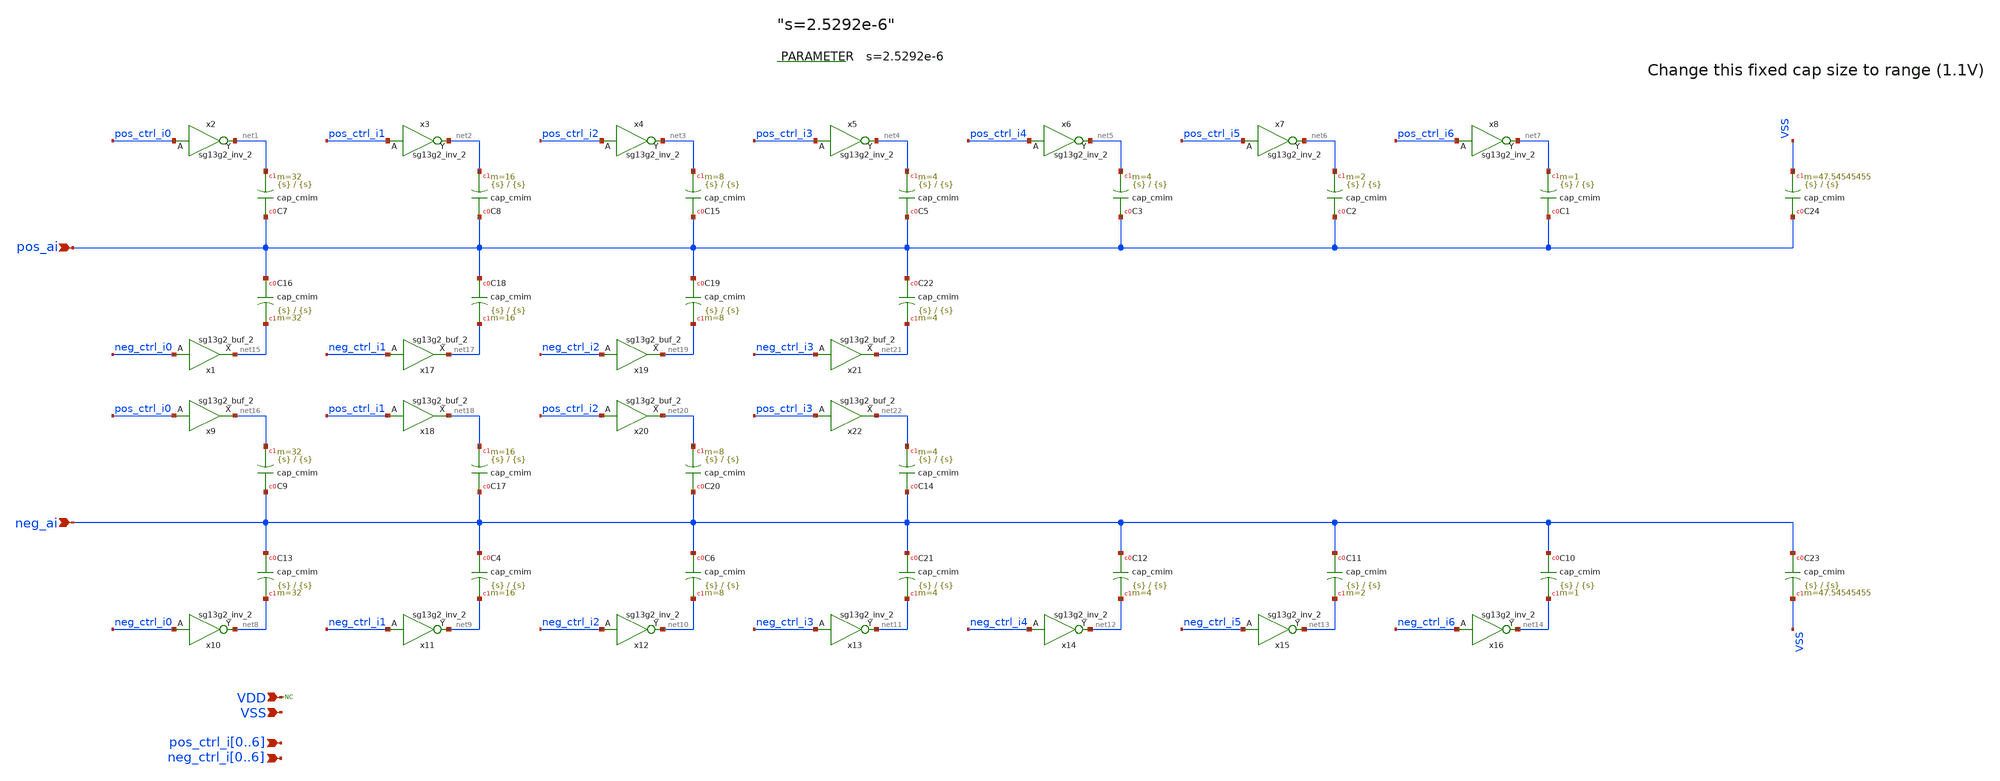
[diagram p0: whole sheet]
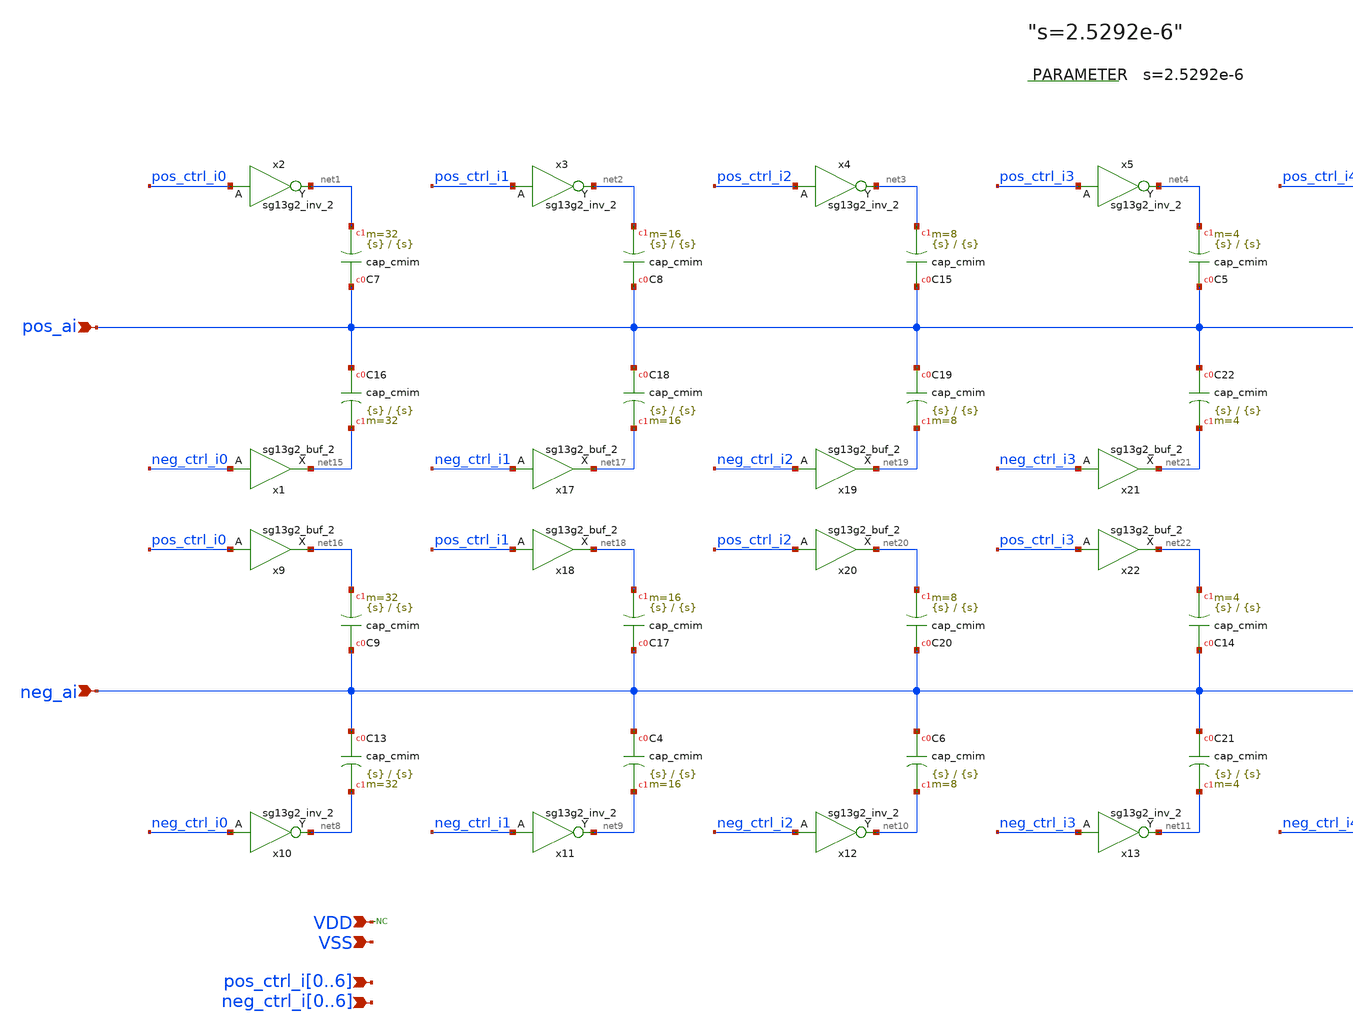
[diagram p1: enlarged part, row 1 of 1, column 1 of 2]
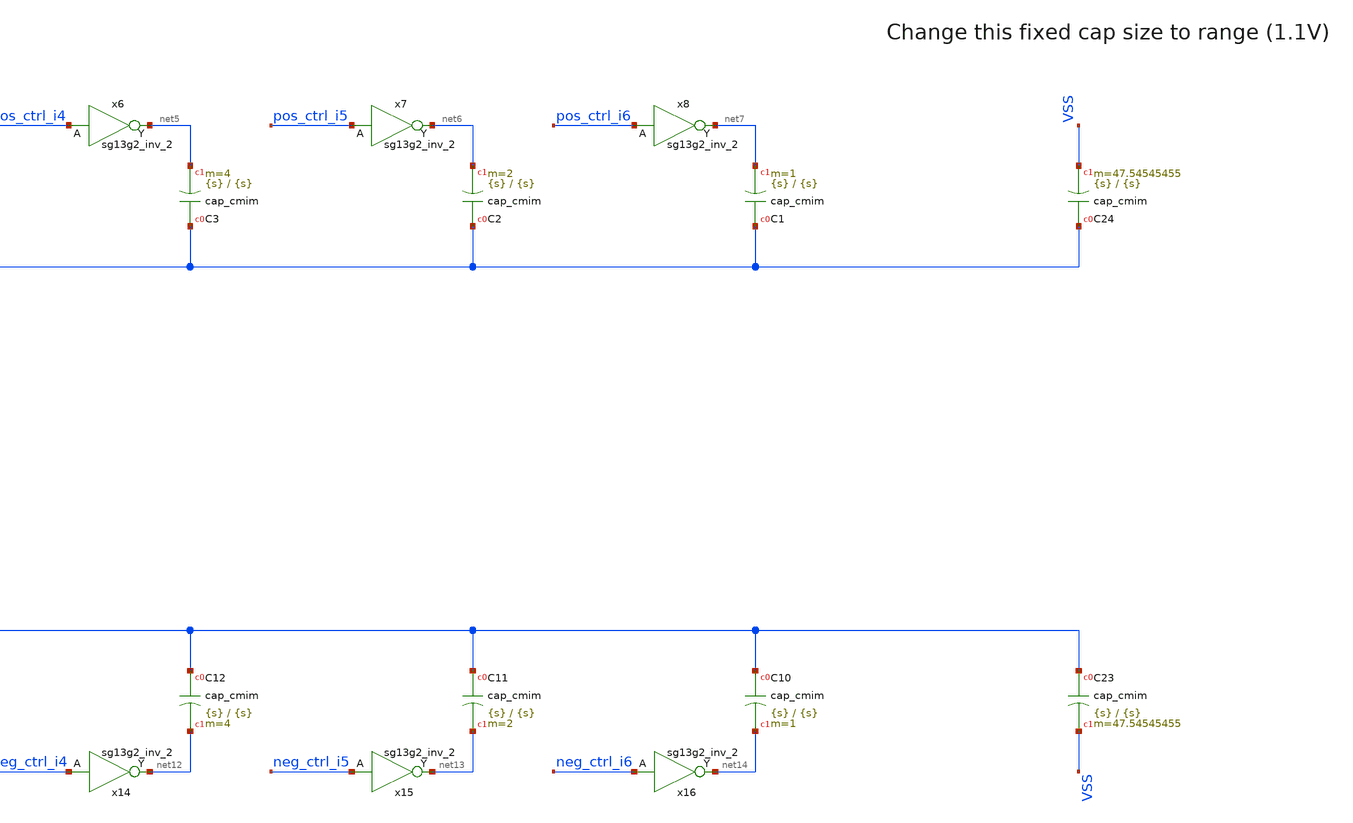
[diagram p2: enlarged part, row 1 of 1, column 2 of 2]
** sch_path: xschem/cdac.sch
* IHP-GmbH/IHP-Open-PDK/ihp-sg13g2/libs.tech/xschem/sg13g2_stdcells/sg13g2_inv_2.sch:
* Copyright 2023 IHP PDK Authors
* Licensed under the Apache License, Version 2.0 (the "License");
**.subckt cdac pos_ai VSS VDD neg_ai
*+ pos_ctrl_i0,pos_ctrl_i1,pos_ctrl_i2,pos_ctrl_i3,pos_ctrl_i4,pos_ctrl_i5,pos_ctrl_i6 neg_ctrl_i0,neg_ctrl_i1,neg_ctrl_i2,neg_ctrl_i3,neg_ctrl_i4,neg_ctrl_i5,neg_ctrl_i6
*.ipin pos_ai
*.ipin VSS
*.ipin VDD
*.ipin neg_ai
*.ipin pos_ctrl_i0,pos_ctrl_i1,pos_ctrl_i2,pos_ctrl_i3,pos_ctrl_i4,pos_ctrl_i5,pos_ctrl_i6
*.ipin neg_ctrl_i0,neg_ctrl_i1,neg_ctrl_i2,neg_ctrl_i3,neg_ctrl_i4,neg_ctrl_i5,neg_ctrl_i6
x2 net1 pos_ctrl_i0 VDD VSS sg13g2_inv_2
x3 net2 pos_ctrl_i1 VDD VSS sg13g2_inv_2
x4 net3 pos_ctrl_i2 VDD VSS sg13g2_inv_2
x5 net4 pos_ctrl_i3 VDD VSS sg13g2_inv_2
x6 net5 pos_ctrl_i4 VDD VSS sg13g2_inv_2
x7 net6 pos_ctrl_i5 VDD VSS sg13g2_inv_2
x8 net7 pos_ctrl_i6 VDD VSS sg13g2_inv_2
XC1 pos_ai net7 cap_cmim w={s} l={s} m=1 mm_ok=1
XC2 pos_ai net6 cap_cmim w={s} l={s} m=2 mm_ok=1
XC3 pos_ai net5 cap_cmim w={s} l={s} m=4 mm_ok=1
x10 net8 neg_ctrl_i0 VDD VSS sg13g2_inv_2
x11 net9 neg_ctrl_i1 VDD VSS sg13g2_inv_2
x12 net10 neg_ctrl_i2 VDD VSS sg13g2_inv_2
x13 net11 neg_ctrl_i3 VDD VSS sg13g2_inv_2
x14 net12 neg_ctrl_i4 VDD VSS sg13g2_inv_2
x15 net13 neg_ctrl_i5 VDD VSS sg13g2_inv_2
x16 net14 neg_ctrl_i6 VDD VSS sg13g2_inv_2
XC10 neg_ai net14 cap_cmim w={s} l={s} m=1 mm_ok=1
XC11 neg_ai net13 cap_cmim w={s} l={s} m=2 mm_ok=1
XC12 neg_ai net12 cap_cmim w={s} l={s} m=4 mm_ok=1
* noconn VDD
.param s=2.5292e-6
x1 net15 neg_ctrl_i0 VDD VSS sg13g2_buf_2
x9 net16 pos_ctrl_i0 VDD VSS sg13g2_buf_2
XC7 pos_ai net1 cap_cmim w={s} l={s} m=32 mm_ok=1
XC9 neg_ai net16 cap_cmim w={s} l={s} m=32 mm_ok=1
XC13 neg_ai net8 cap_cmim w={s} l={s} m=32 mm_ok=1
XC16 pos_ai net15 cap_cmim w={s} l={s} m=32 mm_ok=1
x17 net17 neg_ctrl_i1 VDD VSS sg13g2_buf_2
x18 net18 pos_ctrl_i1 VDD VSS sg13g2_buf_2
XC17 neg_ai net18 cap_cmim w={s} l={s} m=16 mm_ok=1
XC18 pos_ai net17 cap_cmim w={s} l={s} m=16 mm_ok=1
XC4 neg_ai net9 cap_cmim w={s} l={s} m=16 mm_ok=1
XC8 pos_ai net2 cap_cmim w={s} l={s} m=16 mm_ok=1
x19 net19 neg_ctrl_i2 VDD VSS sg13g2_buf_2
x20 net20 pos_ctrl_i2 VDD VSS sg13g2_buf_2
XC19 pos_ai net19 cap_cmim w={s} l={s} m=8 mm_ok=1
XC6 neg_ai net10 cap_cmim w={s} l={s} m=8 mm_ok=1
XC15 pos_ai net3 cap_cmim w={s} l={s} m=8 mm_ok=1
XC20 neg_ai net20 cap_cmim w={s} l={s} m=8 mm_ok=1
x21 net21 neg_ctrl_i3 VDD VSS sg13g2_buf_2
x22 net22 pos_ctrl_i3 VDD VSS sg13g2_buf_2
XC5 pos_ai net4 cap_cmim w={s} l={s} m=4 mm_ok=1
XC14 neg_ai net22 cap_cmim w={s} l={s} m=4 mm_ok=1
XC21 neg_ai net11 cap_cmim w={s} l={s} m=4 mm_ok=1
XC22 pos_ai net21 cap_cmim w={s} l={s} m=4 mm_ok=1
XC23 neg_ai VSS cap_cmim w={s} l={s} m=47.54545455 mm_ok=1
XC24 pos_ai VSS cap_cmim w={s} l={s} m=47.54545455 mm_ok=1
**.ends

* expanding   symbol:  sg13g2_stdcells/sg13g2_inv_2.sym # of pins=2
** sym_path: sg13g2_stdcells/sg13g2_inv_2.sym
** sch_path: sg13g2_stdcells/sg13g2_inv_2.sch
.subckt sg13g2_inv_2 Y A VDD VSS
*.opin Y
*.ipin A
*.iopin VDD
*.iopin VSS
XM1 Y A VSS VSS sg13_lv_nmos w=1.48u l=130.00n ng=2 m=1 mm_ok=1
XM2 Y A VDD VDD sg13_lv_pmos w=2.24u l=130.00n ng=2 m=1 mm_ok=1
.ends


* expanding   symbol:  sg13g2_stdcells/sg13g2_buf_2.sym # of pins=2
** sym_path: sg13g2_stdcells/sg13g2_buf_2.sym
** sch_path: sg13g2_stdcells/sg13g2_buf_2.sch
.subckt sg13g2_buf_2 X A VDD VSS
*.ipin A
*.opin X
*.iopin VDD
*.iopin VSS
XM1 net1 A VSS VSS sg13_lv_nmos w=640.00n l=130.00n ng=1 m=1 mm_ok=1
XM2 X net1 VSS VSS sg13_lv_nmos w=1.48u l=130.00n ng=2 m=1 mm_ok=1
XM3 net1 A VDD VDD sg13_lv_pmos w=1.000u l=130.00n ng=1 m=1 mm_ok=1
XM4 X net1 VDD VDD sg13_lv_pmos w=2.24u l=130.00n ng=2 m=1 mm_ok=1
.ends

.end
